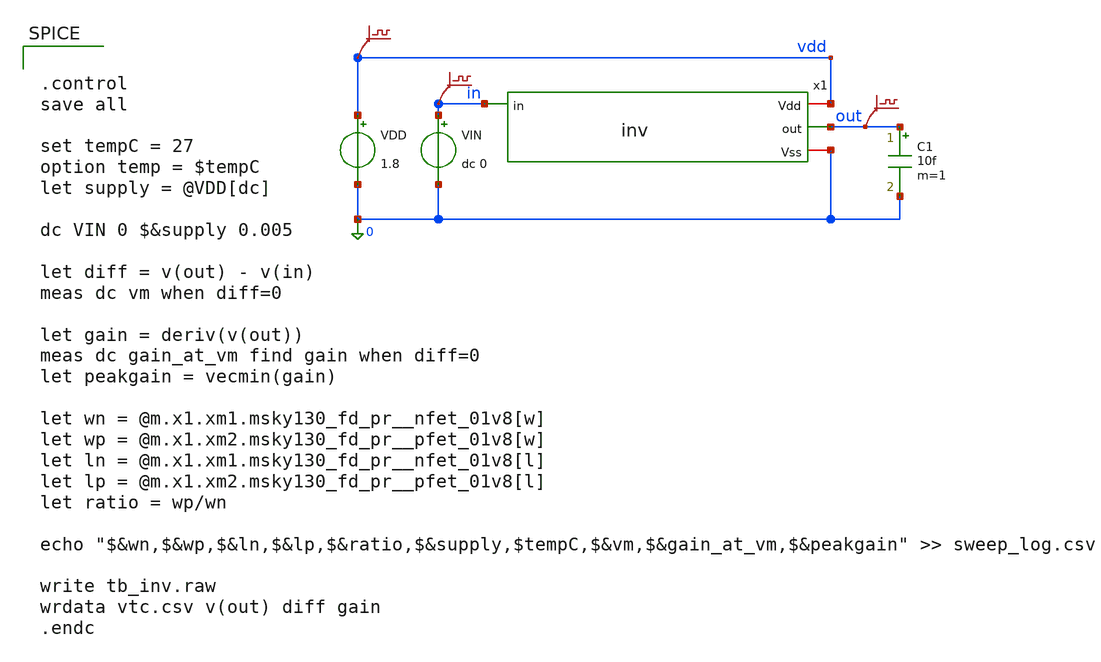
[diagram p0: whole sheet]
** sch_path: sandbox/inv-experimental/tb_inv.sch
**.subckt tb_inv
x1 vdd out in 0 inv
VDD vdd 0 1.8
VIN in 0 dc 0
C1 out 0 10f m=1
.save v(vdd)
.save v(in)
.save v(out)
**** begin user architecture code
 ** opencircuitdesign pdks install
.lib $::SKYWATER_MODELS/sky130.lib.spice tt

.param mc_mm_switch=0
.param mc_pr_switch=0



.control
save all

set tempC = 27
option temp = $tempC
let supply = @VDD[dc]

dc VIN 0 $&supply 0.005

let diff = v(out) - v(in)
meas dc vm when diff=0

let gain = deriv(v(out))
meas dc gain_at_vm find gain when diff=0
let peakgain = vecmin(gain)

let wn = @m.x1.xm1.msky130_fd_pr__nfet_01v8[w]
let wp = @m.x1.xm2.msky130_fd_pr__pfet_01v8[w]
let ln = @m.x1.xm1.msky130_fd_pr__nfet_01v8[l]
let lp = @m.x1.xm2.msky130_fd_pr__pfet_01v8[l]
let ratio = wp/wn

echo "$&wn,$&wp,$&ln,$&lp,$&ratio,$&supply,$tempC,$&vm,$&gain_at_vm,$&peakgain" >> sweep_log.csv

write tb_inv.raw
wrdata vtc.csv v(out) diff gain
.endc


**** end user architecture code
**.ends

* expanding   symbol:  inv.sym # of pins=4
** sym_path: sandbox/inv-experimental/inv.sym
** sch_path: sandbox/inv-experimental/inv.sch
.subckt inv Vdd out in Vss
*.ipin in
*.iopin Vdd
*.opin out
*.iopin Vss
XM1 out in Vss Vss sky130_fd_pr__nfet_01v8 L=0.15 W=1 nf=1 ad='int((1 + 1)/2) * 1 / 1 * 0.29' as='int((1 + 2)/2) * 1 / 1 * 0.29'
+ pd='2*int((1 + 1)/2) * (1 / 1 + 0.29)' ps='2*int((1 + 2)/2) * (1 / 1 + 0.29)' nrd='0.29 / 1 ' nrs='0.29 / 1 '
+ sa=0 sb=0 sd=0 mult=1 m=1
XM2 out in Vdd Vdd sky130_fd_pr__pfet_01v8 L=0.15 W=1 nf=1 ad='int((1 + 1)/2) * 1 / 1 * 0.29' as='int((1 + 2)/2) * 1 / 1 * 0.29'
+ pd='2*int((1 + 1)/2) * (1 / 1 + 0.29)' ps='2*int((1 + 2)/2) * (1 / 1 + 0.29)' nrd='0.29 / 1 ' nrs='0.29 / 1 '
+ sa=0 sb=0 sd=0 mult=1 m=1
.ends

.end
